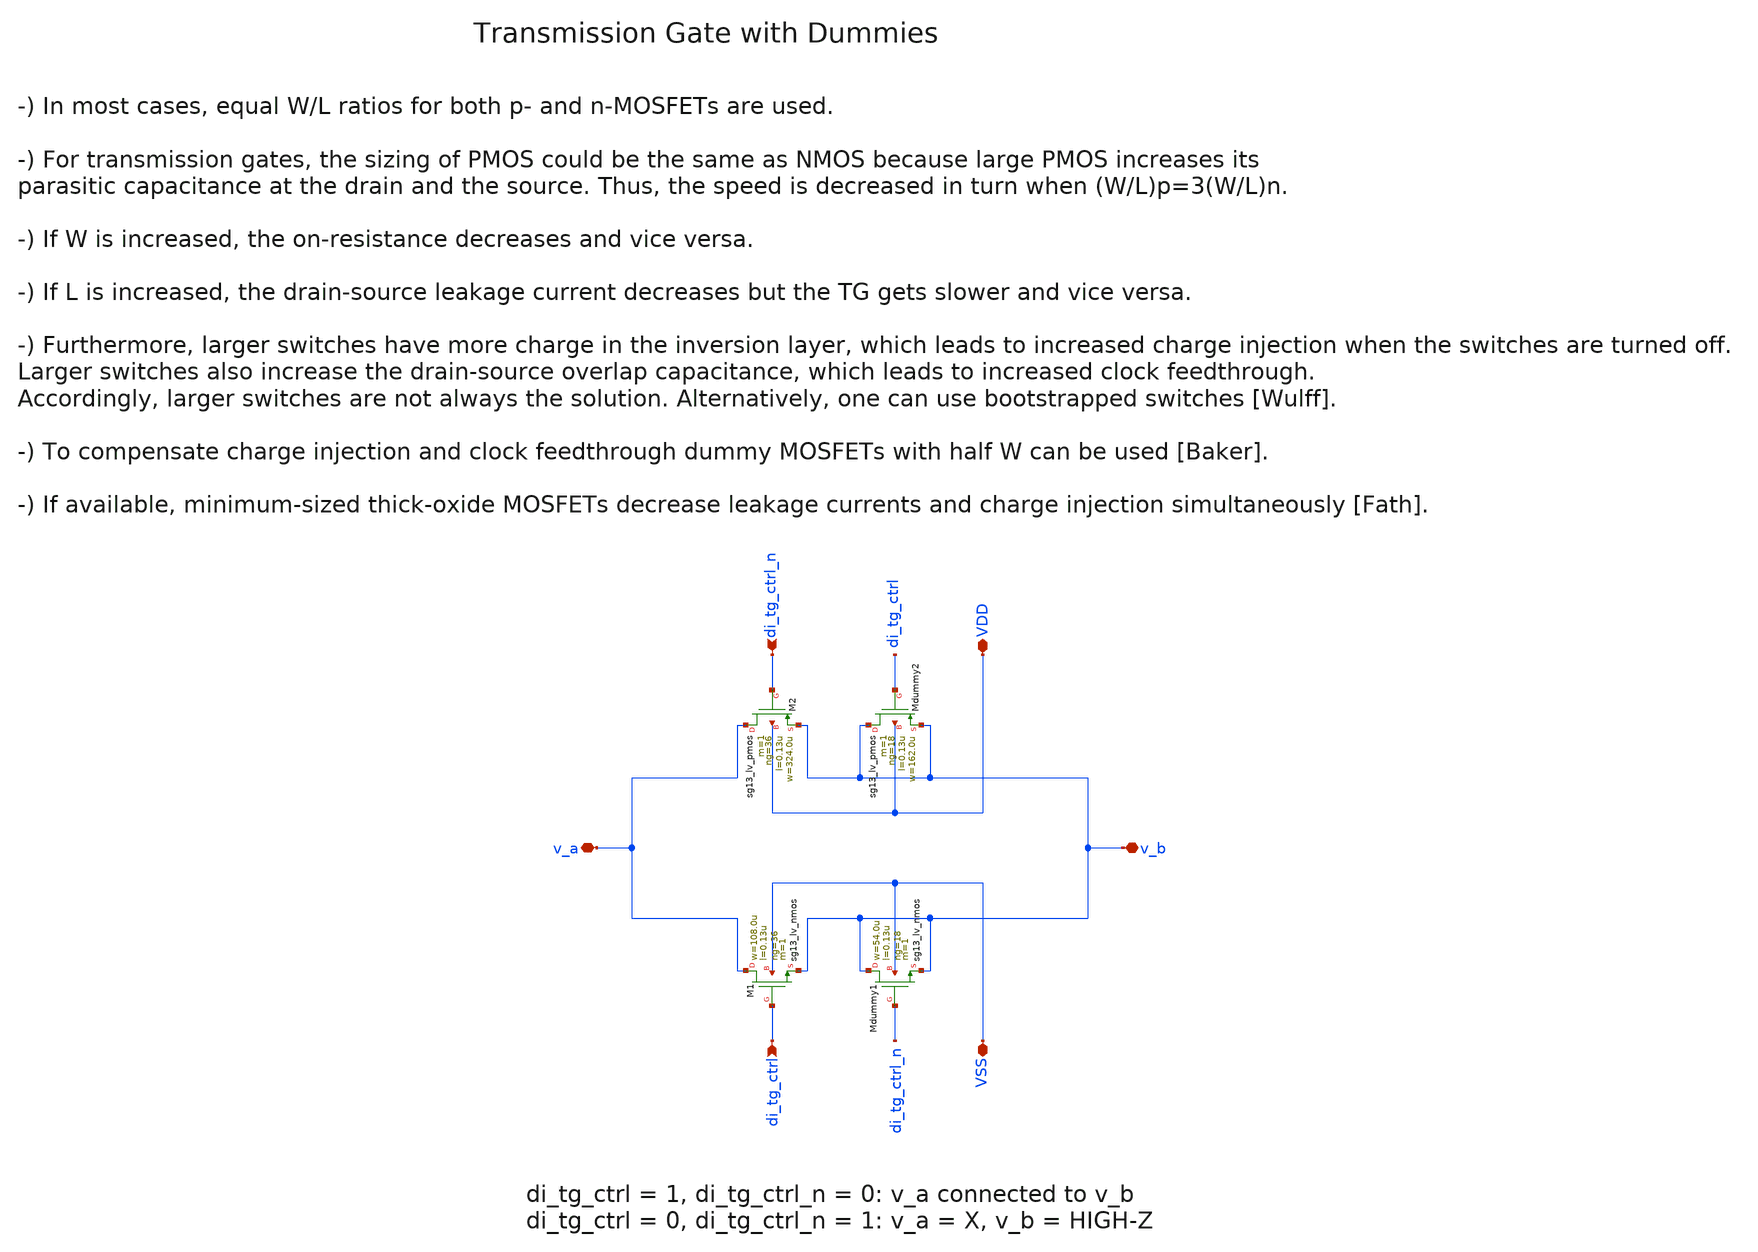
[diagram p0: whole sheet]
** sch_path: ihp130/macros/iqmod/schematic/xschem/iqmod_mixer_tg.sch
**.subckt iqmod_mixer_tg v_a v_b di_tg_ctrl di_tg_ctrl_n VDD VSS
*.iopin v_a
*.iopin v_b
*.ipin di_tg_ctrl
*.ipin di_tg_ctrl_n
*.iopin VDD
*.iopin VSS
XM1 v_a di_tg_ctrl v_b VSS sg13_lv_nmos w=108.0u l=0.13u ng=36 m=1 mm_ok=1
XM2 v_a di_tg_ctrl_n v_b VDD sg13_lv_pmos w=324.0u l=0.13u ng=36 m=1 mm_ok=1
XMdummy2 v_b di_tg_ctrl v_b VDD sg13_lv_pmos w=162.0u l=0.13u ng=18 m=1 mm_ok=1
XMdummy1 v_b di_tg_ctrl_n v_b VSS sg13_lv_nmos w=54.0u l=0.13u ng=18 m=1 mm_ok=1
**.ends
.end
